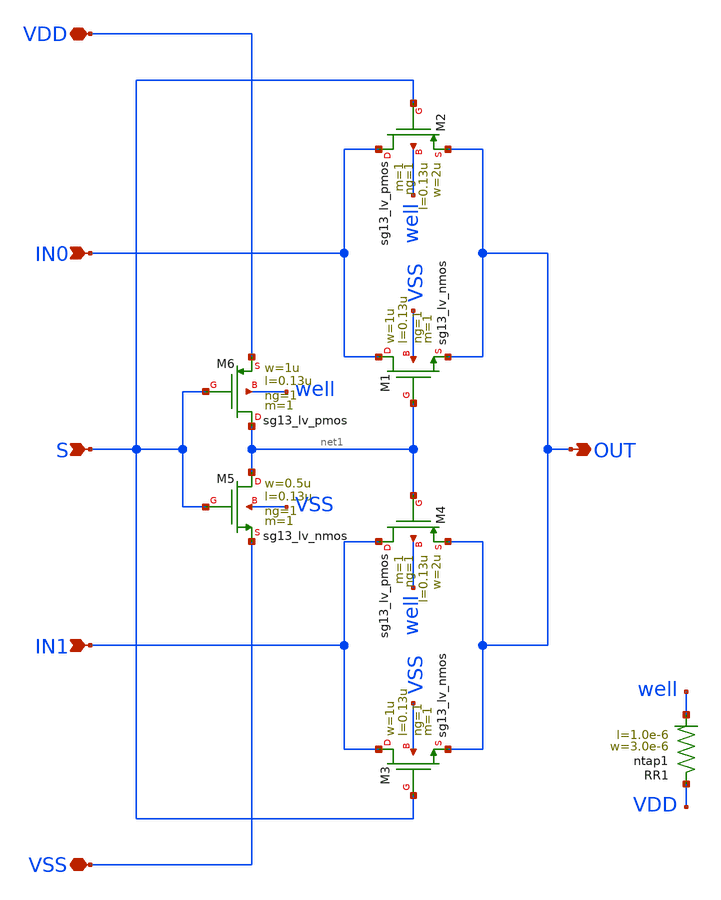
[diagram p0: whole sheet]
** sch_path: Layouts/mux/mux.sch
**.subckt mux S IN0 IN1 OUT VDD VSS
*.ipin S
*.ipin IN0
*.ipin IN1
*.opin OUT
*.iopin VDD
*.iopin VSS
XM1 IN0 net1 OUT VSS sg13_lv_nmos w=1u l=0.13u ng=1 m=1 mm_ok=1
XM2 IN0 S OUT well sg13_lv_pmos w=2u l=0.13u ng=1 m=1 mm_ok=1
XM3 IN1 S OUT VSS sg13_lv_nmos w=1u l=0.13u ng=1 m=1 mm_ok=1
XM4 IN1 net1 OUT well sg13_lv_pmos w=2u l=0.13u ng=1 m=1 mm_ok=1
XR1 VDD well ntap1 R=89.09 w=3.0e-6 l=1.0e-6
XM5 net1 S VSS VSS sg13_lv_nmos w=0.5u l=0.13u ng=1 m=1 mm_ok=1
XM6 net1 S VDD well sg13_lv_pmos w=1u l=0.13u ng=1 m=1 mm_ok=1
**.ends
.end
